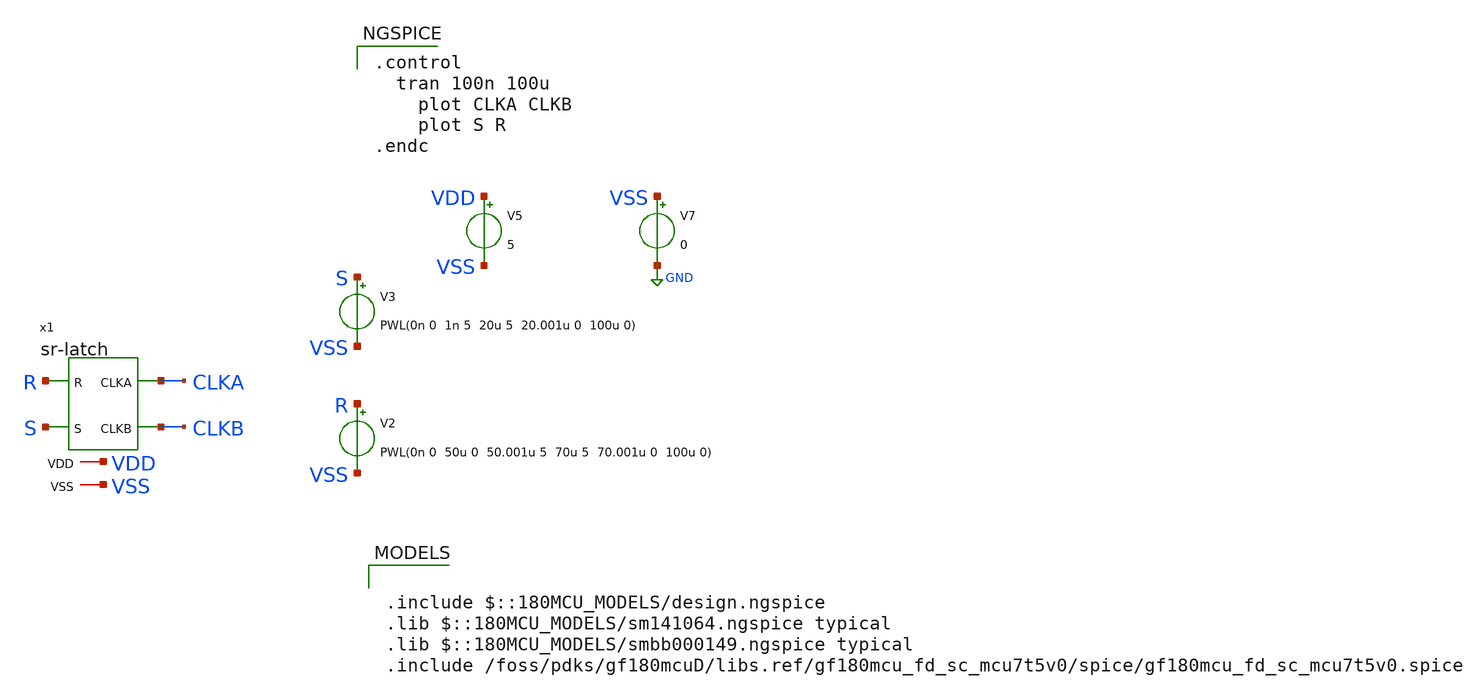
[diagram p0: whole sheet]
** sch_path: designs/relaxation-oscillator/tb-latch.sch
**.subckt tb-latch
V2 R VSS PWL(0n 0 50u 0 50.001u 5 70u 5 70.001u 0 100u 0)
V5 VDD VSS 5
V7 VSS GND 0
V3 S VSS PWL(0n 0 1n 5 20u 5 20.001u 0 100u 0)
x1 VDD R CLKA S CLKB VSS sr-latch
**** begin user architecture code

.control
  tran 100n 100u
	plot CLKA CLKB
	plot S R
.endc




.include $::180MCU_MODELS/design.ngspice
.lib $::180MCU_MODELS/sm141064.ngspice typical
.lib $::180MCU_MODELS/smbb000149.ngspice typical
.include /foss/pdks/gf180mcuD/libs.ref/gf180mcu_fd_sc_mcu7t5v0/spice/gf180mcu_fd_sc_mcu7t5v0.spice

**** end user architecture code
**.ends

* expanding   symbol:  sr-latch.sym # of pins=6
** sym_path: designs/relaxation-oscillator/sr-latch.sym
** sch_path: designs/relaxation-oscillator/sr-latch.sch
.subckt sr-latch VDD R CLKA S CLKB VSS
*.iopin VDD
*.iopin VSS
*.opin CLKA
*.opin CLKB
*.ipin R
*.ipin S
x1 VDD R CLKB CLKA VSS nor
x2 VDD CLKA S CLKB VSS nor
.ends


* expanding   symbol:  nor.sym # of pins=5
** sym_path: designs/relaxation-oscillator/nor.sym
** sch_path: designs/relaxation-oscillator/nor.sch
.subckt nor VDD A B OUT VSS
*.ipin A
*.ipin B
*.iopin VDD
*.iopin VSS
*.opin OUT
XM1 net1 A VDD VDD pfet_05v0 L=0.50u W=0.9u nf=1 ad='int((nf+1)/2) * W/nf * 0.18u' as='int((nf+2)/2) * W/nf * 0.18u'
+ pd='2*int((nf+1)/2) * (W/nf + 0.18u)' ps='2*int((nf+2)/2) * (W/nf + 0.18u)' nrd='0.18u / W' nrs='0.18u / W'
+ sa=0 sb=0 sd=0 m=1
XM2 OUT B net1 VDD pfet_05v0 L=0.50u W=0.9u nf=1 ad='int((nf+1)/2) * W/nf * 0.18u' as='int((nf+2)/2) * W/nf * 0.18u'
+ pd='2*int((nf+1)/2) * (W/nf + 0.18u)' ps='2*int((nf+2)/2) * (W/nf + 0.18u)' nrd='0.18u / W' nrs='0.18u / W'
+ sa=0 sb=0 sd=0 m=1
XM3 OUT A VSS VSS nfet_05v0 L=0.60u W=0.30u nf=1 ad='int((nf+1)/2) * W/nf * 0.18u' as='int((nf+2)/2) * W/nf * 0.18u'
+ pd='2*int((nf+1)/2) * (W/nf + 0.18u)' ps='2*int((nf+2)/2) * (W/nf + 0.18u)' nrd='0.18u / W' nrs='0.18u / W'
+ sa=0 sb=0 sd=0 m=1
XM4 OUT B VSS VSS nfet_05v0 L=0.60u W=0.30u nf=1 ad='int((nf+1)/2) * W/nf * 0.18u' as='int((nf+2)/2) * W/nf * 0.18u'
+ pd='2*int((nf+1)/2) * (W/nf + 0.18u)' ps='2*int((nf+2)/2) * (W/nf + 0.18u)' nrd='0.18u / W' nrs='0.18u / W'
+ sa=0 sb=0 sd=0 m=1
.ends

.GLOBAL GND
.end
